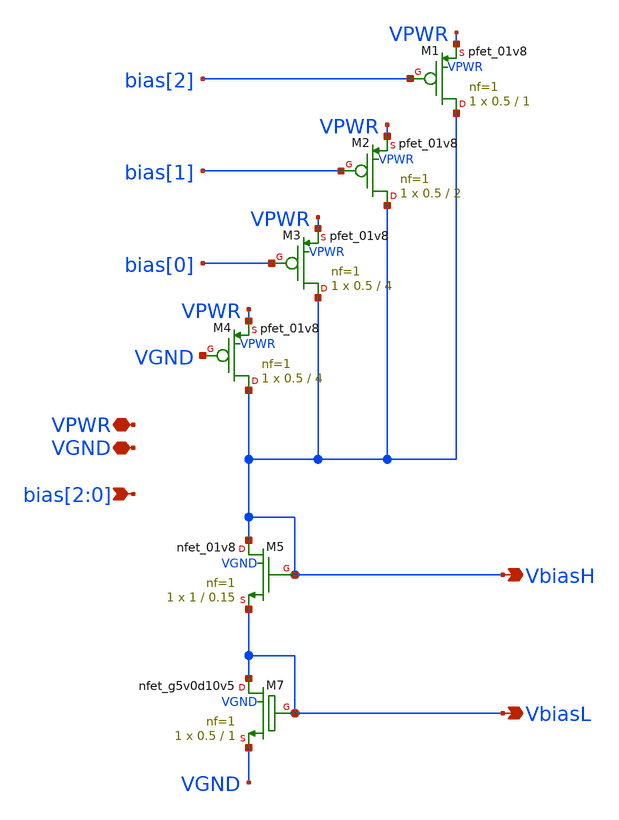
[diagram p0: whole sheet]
** sch_path: xschem-cascode-backup/vbiasM5.sch
**.subckt vbiasM5 VPWR VGND bias[2],bias[1],bias[0] VbiasH VbiasL
*.iopin VPWR
*.iopin VGND
*.ipin bias[2],bias[1],bias[0]
*.opin VbiasH
*.opin VbiasL
XM1 VbiasH bias[2] VPWR VPWR sky130_fd_pr__pfet_01v8 L=1 W=0.5 nf=1 ad='int((nf+1)/2) * W/nf * 0.29'
+ as='int((nf+2)/2) * W/nf * 0.29' pd='2*int((nf+1)/2) * (W/nf + 0.29)' ps='2*int((nf+2)/2) * (W/nf + 0.29)'
+ nrd='0.29 / W' nrs='0.29 / W' sa=0 sb=0 sd=0 mult=1 m=1
XM2 VbiasH bias[1] VPWR VPWR sky130_fd_pr__pfet_01v8 L=2 W=0.5 nf=1 ad='int((nf+1)/2) * W/nf * 0.29'
+ as='int((nf+2)/2) * W/nf * 0.29' pd='2*int((nf+1)/2) * (W/nf + 0.29)' ps='2*int((nf+2)/2) * (W/nf + 0.29)'
+ nrd='0.29 / W' nrs='0.29 / W' sa=0 sb=0 sd=0 mult=1 m=1
XM3 VbiasH bias[0] VPWR VPWR sky130_fd_pr__pfet_01v8 L=4 W=0.5 nf=1 ad='int((nf+1)/2) * W/nf * 0.29'
+ as='int((nf+2)/2) * W/nf * 0.29' pd='2*int((nf+1)/2) * (W/nf + 0.29)' ps='2*int((nf+2)/2) * (W/nf + 0.29)'
+ nrd='0.29 / W' nrs='0.29 / W' sa=0 sb=0 sd=0 mult=1 m=1
XM4 VbiasH VGND VPWR VPWR sky130_fd_pr__pfet_01v8 L=4 W=0.5 nf=1 ad='int((nf+1)/2) * W/nf * 0.29' as='int((nf+2)/2) * W/nf * 0.29'
+ pd='2*int((nf+1)/2) * (W/nf + 0.29)' ps='2*int((nf+2)/2) * (W/nf + 0.29)' nrd='0.29 / W' nrs='0.29 / W'
+ sa=0 sb=0 sd=0 mult=1 m=1
XM7 VbiasL VbiasL VGND VGND sky130_fd_pr__nfet_g5v0d10v5 L=1 W=0.5 nf=1 ad='int((nf+1)/2) * W/nf * 0.29'
+ as='int((nf+2)/2) * W/nf * 0.29' pd='2*int((nf+1)/2) * (W/nf + 0.29)' ps='2*int((nf+2)/2) * (W/nf + 0.29)'
+ nrd='0.29 / W' nrs='0.29 / W' sa=0 sb=0 sd=0 mult=1 m=1
XM5 VbiasH VbiasH VbiasL VGND sky130_fd_pr__nfet_01v8 L=0.15 W=1 nf=1 ad='int((nf+1)/2) * W/nf * 0.29'
+ as='int((nf+2)/2) * W/nf * 0.29' pd='2*int((nf+1)/2) * (W/nf + 0.29)' ps='2*int((nf+2)/2) * (W/nf + 0.29)'
+ nrd='0.29 / W' nrs='0.29 / W' sa=0 sb=0 sd=0 mult=1 m=1
**.ends
.end
